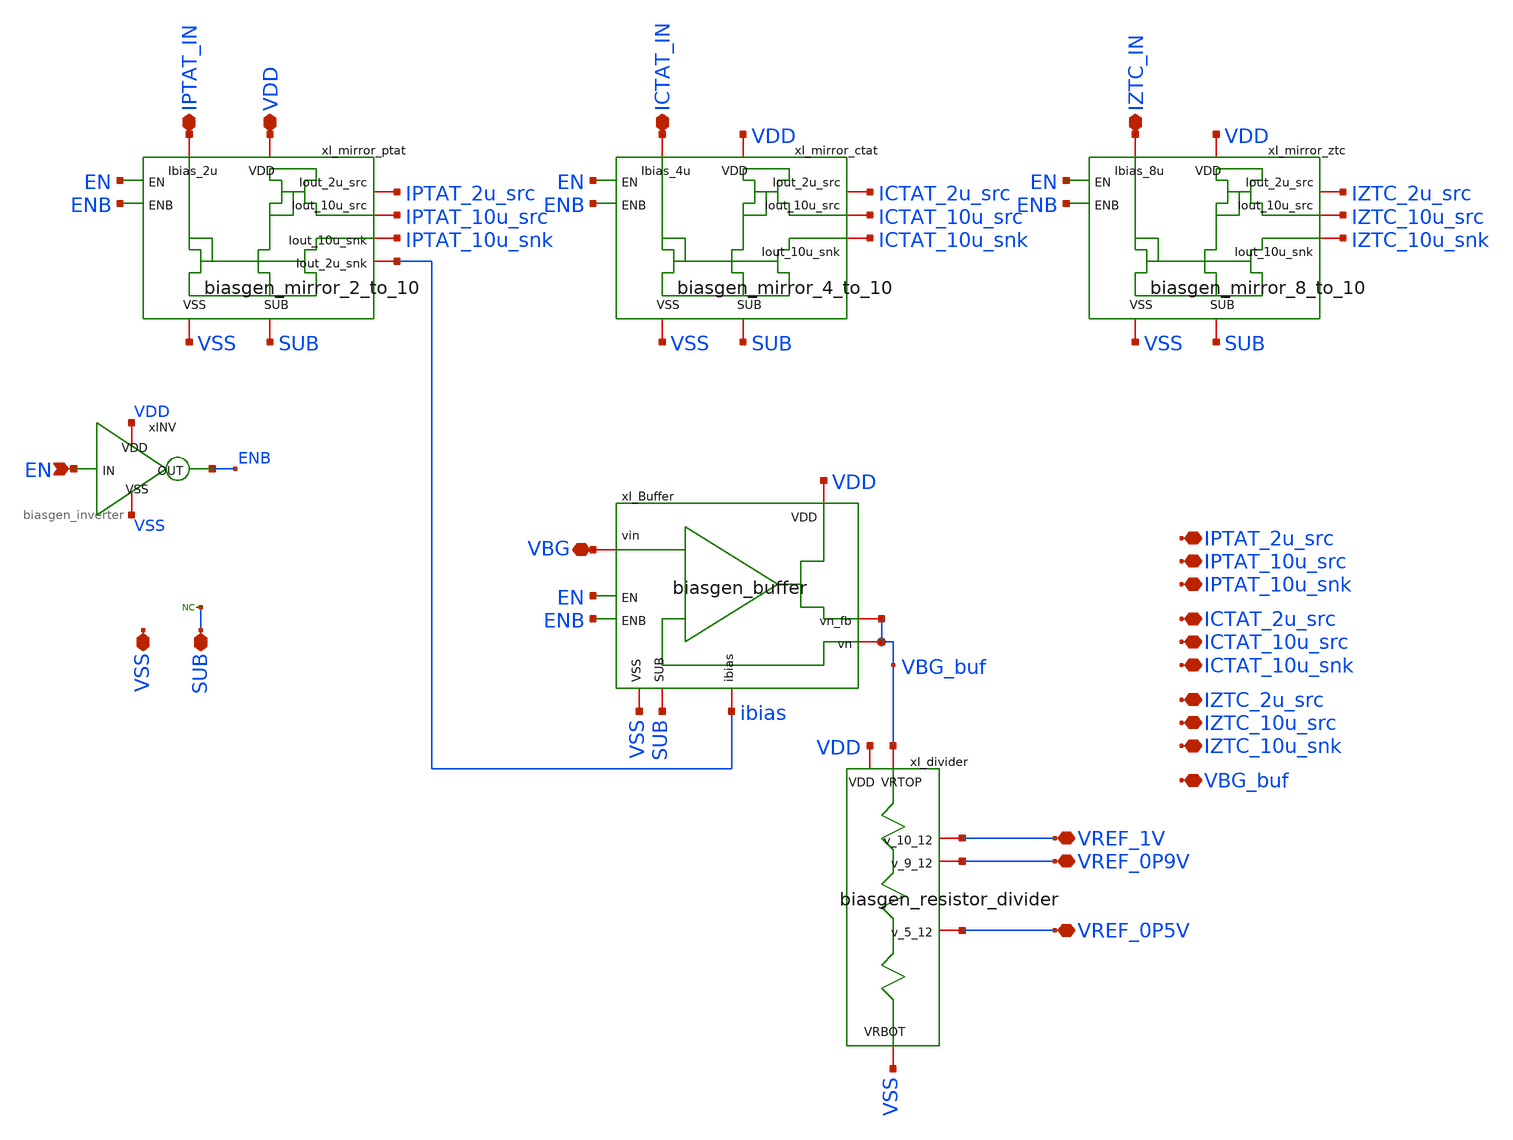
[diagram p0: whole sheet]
** sch_path: designs/libs/core_biasgen/biasgen/biasgen.sch
**.subckt biasgen VSS SUB VBG IPTAT_IN IZTC_IN VREF_0P9V VREF_0P5V IPTAT_2u_src IPTAT_10u_snk
*+ ICTAT_IN VDD EN VREF_1V IPTAT_10u_src ICTAT_2u_src ICTAT_10u_snk ICTAT_10u_src IZTC_2u_src IZTC_10u_snk
*+ IZTC_10u_src VBG_buf
*.iopin VSS
*.iopin SUB
*.iopin VBG
*.iopin IPTAT_IN
*.iopin IZTC_IN
*.iopin VREF_0P9V
*.iopin VREF_0P5V
*.iopin IPTAT_2u_src
*.iopin IPTAT_10u_snk
*.iopin ICTAT_IN
*.iopin VDD
*.ipin EN
*.iopin VREF_1V
*.iopin IPTAT_10u_src
*.iopin ICTAT_2u_src
*.iopin ICTAT_10u_snk
*.iopin ICTAT_10u_src
*.iopin IZTC_2u_src
*.iopin IZTC_10u_snk
*.iopin IZTC_10u_src
*.iopin VBG_buf
* noconn SUB
xI_Buffer VDD EN ENB VBG SUB ibias VBG_buf VBG_buf VSS biasgen_buffer
xI_mirror_ptat VDD IPTAT_IN EN ENB IPTAT_10u_src IPTAT_10u_snk VSS SUB IPTAT_2u_src ibias
+ biasgen_mirror_2_to_10
xI_mirror_ctat VDD ICTAT_IN EN ENB ICTAT_10u_src ICTAT_10u_snk VSS SUB ICTAT_2u_src
+ biasgen_mirror_4_to_10
xI_mirror_ztc VDD IZTC_IN EN ENB IZTC_10u_src IZTC_10u_snk VSS SUB IZTC_2u_src
+ biasgen_mirror_8_to_10
xI_divider VBG_buf VDD VREF_1V VREF_0P9V VREF_0P5V VSS biasgen_resistor_divider
xINV VDD EN ENB VSS biasgen_inverter
**.ends
.end
